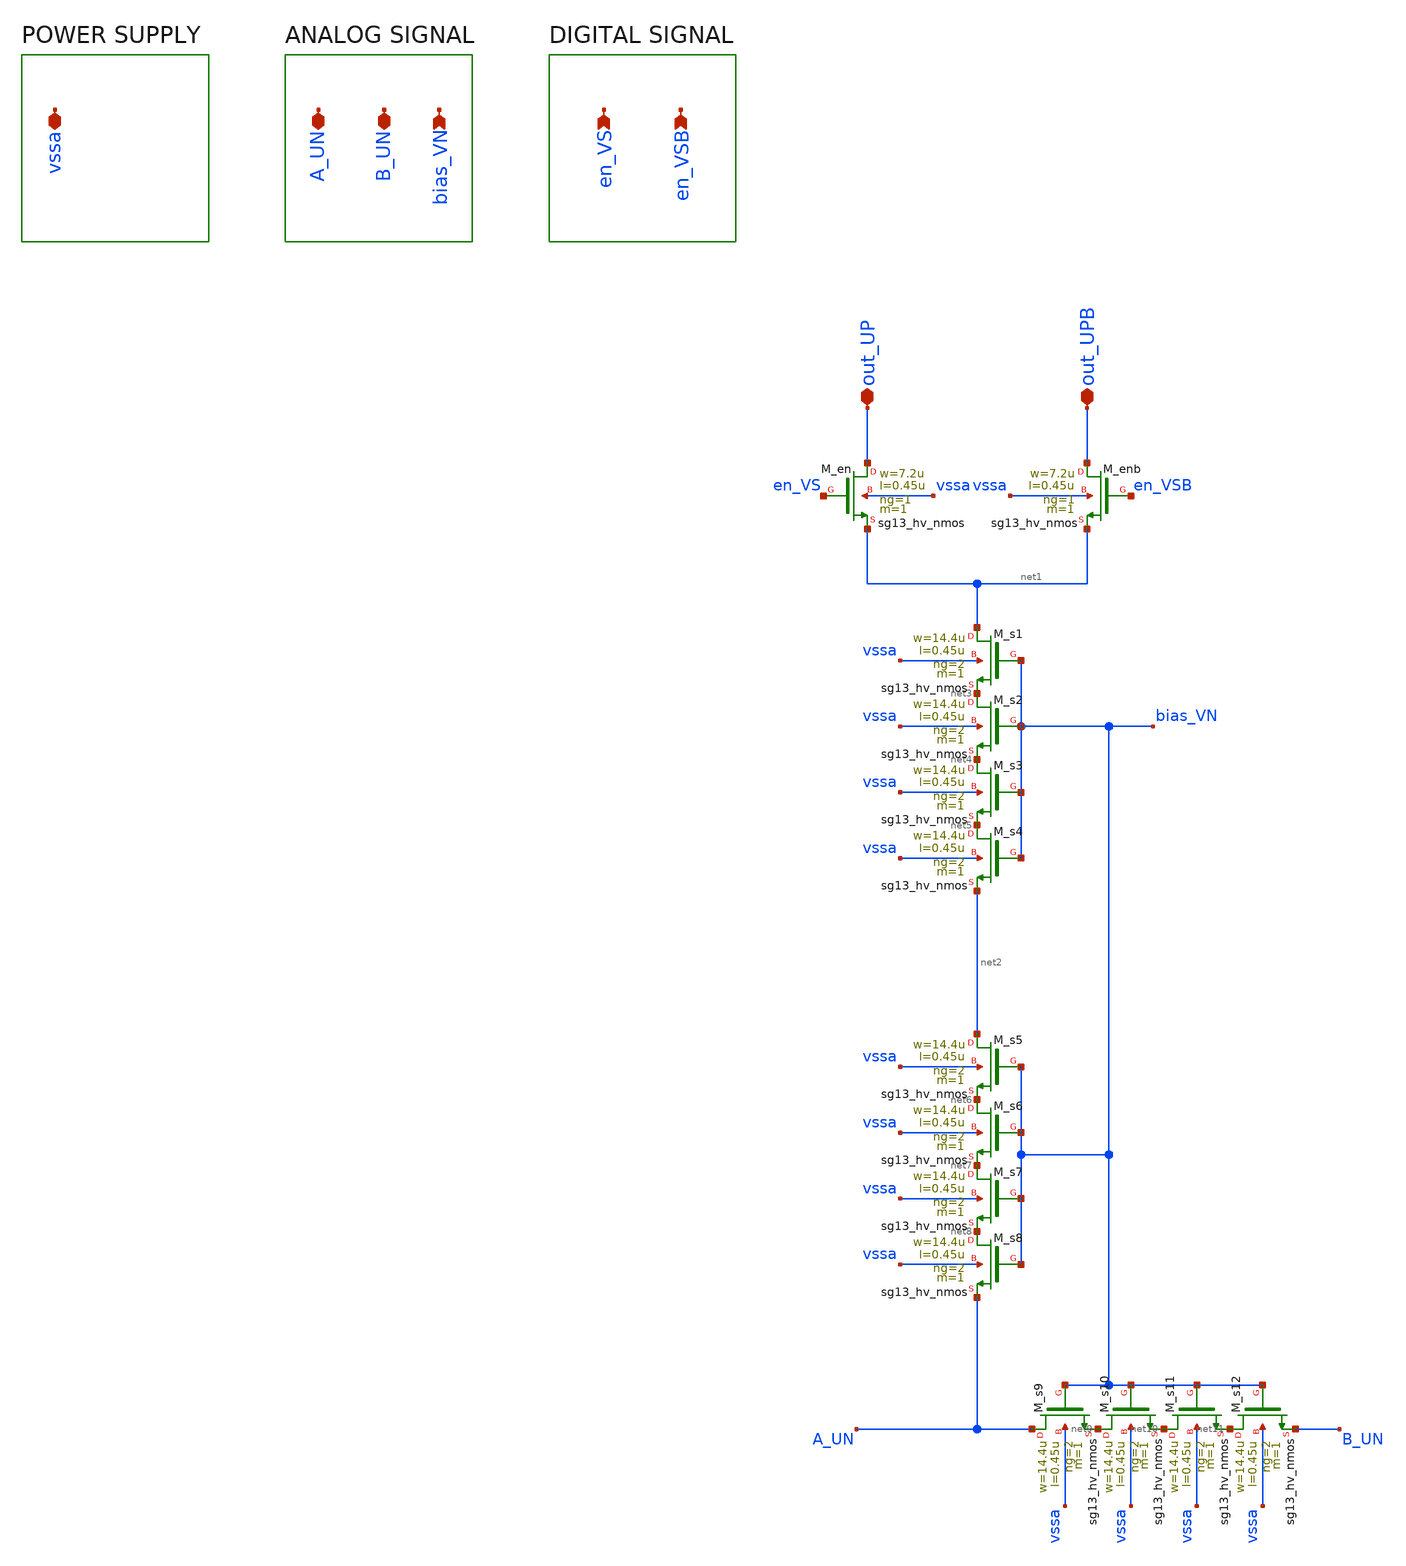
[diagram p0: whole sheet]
** sch_path: SplitterCell.sch
**.subckt SplitterCell en_VS en_VSB bias_VN B_UN out_UP out_UPB vssa A_UN
*.ipin en_VS
*.ipin en_VSB
*.ipin bias_VN
*.iopin B_UN
*.iopin out_UP
*.iopin out_UPB
*.iopin vssa
*.iopin A_UN
XM_en out_UP en_VS net1 vssa sg13_hv_nmos w=7.2u l=0.45u ng=1 m=1 mm_ok=1
XM_enb out_UPB en_VSB net1 vssa sg13_hv_nmos w=7.2u l=0.45u ng=1 m=1 mm_ok=1
XM_s1 net1 bias_VN net3 vssa sg13_hv_nmos w=14.4u l=0.45u ng=2 m=1 mm_ok=1
XM_s2 net3 bias_VN net4 vssa sg13_hv_nmos w=14.4u l=0.45u ng=2 m=1 mm_ok=1
XM_s3 net4 bias_VN net5 vssa sg13_hv_nmos w=14.4u l=0.45u ng=2 m=1 mm_ok=1
XM_s4 net5 bias_VN net2 vssa sg13_hv_nmos w=14.4u l=0.45u ng=2 m=1 mm_ok=1
XM_s5 net2 bias_VN net6 vssa sg13_hv_nmos w=14.4u l=0.45u ng=2 m=1 mm_ok=1
XM_s6 net6 bias_VN net7 vssa sg13_hv_nmos w=14.4u l=0.45u ng=2 m=1 mm_ok=1
XM_s7 net7 bias_VN net8 vssa sg13_hv_nmos w=14.4u l=0.45u ng=2 m=1 mm_ok=1
XM_s8 net8 bias_VN A_UN vssa sg13_hv_nmos w=14.4u l=0.45u ng=2 m=1 mm_ok=1
XM_s9 A_UN bias_VN net9 vssa sg13_hv_nmos w=14.4u l=0.45u ng=2 m=1 mm_ok=1
XM_s10 net9 bias_VN net10 vssa sg13_hv_nmos w=14.4u l=0.45u ng=2 m=1 mm_ok=1
XM_s11 net10 bias_VN net11 vssa sg13_hv_nmos w=14.4u l=0.45u ng=2 m=1 mm_ok=1
XM_s12 net11 bias_VN B_UN vssa sg13_hv_nmos w=14.4u l=0.45u ng=2 m=1 mm_ok=1
**.ends
.end
